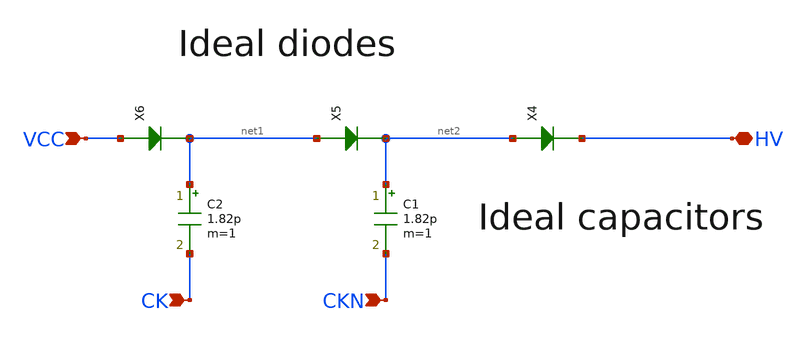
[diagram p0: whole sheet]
** sch_path: sky130A/xschem_libs/sky130_tests/charge_pump_ideal/schematic/charge_pump_ideal.sch
* Copyright 2021 Stefan Frederik Schippers
* Licensed under the Apache License, Version 2.0 (the "License");
* you may not use this file except in compliance with the License.
* You may obtain a copy of the License at
* https://www.apache.org/licenses/LICENSE-2.0
* Unless required by applicable law or agreed to in writing, software
* distributed under the License is distributed on an "AS IS" BASIS,
* WITHOUT WARRANTIES OR CONDITIONS OF ANY KIND, either express or implied.
* See the License for the specific language governing permissions and
* limitations under the License.
**.subckt charge_pump_ideal CK CKN HV VCC
*.ipin CK
*.ipin CKN
*.iopin HV
*.ipin VCC
X4 net2 HV diode_ngspice Ron=0.1 Roff=1e9 m=1
X5 net1 net2 diode_ngspice Ron=0.1 Roff=1e9 m=1
X6 VCC net1 diode_ngspice Ron=0.1 Roff=1e9 m=1
C1 net2 CKN 1.82p m=1
C2 net1 CK 1.82p m=1
**.ends

* expanding   symbol:  sky130_tests/diode_ngspice.sym # of pins=2
** sym_path: sky130_tests/diode_ngspice.sym
** sch_path: sky130_tests/diode_ngspice.sch
.subckt diode_ngspice plus minus   Roff=1e9 Ron=0.1
*.iopin plus
*.iopin minus
Vm mn minus 0
.save i(vm)
Vp plus pn 0
.save i(vp)
B1 pn mn I = 'v(pn,mn) > 0 ? v(pn,mn) / Ron : v(pn,mn) / Roff'
.ends

.end
